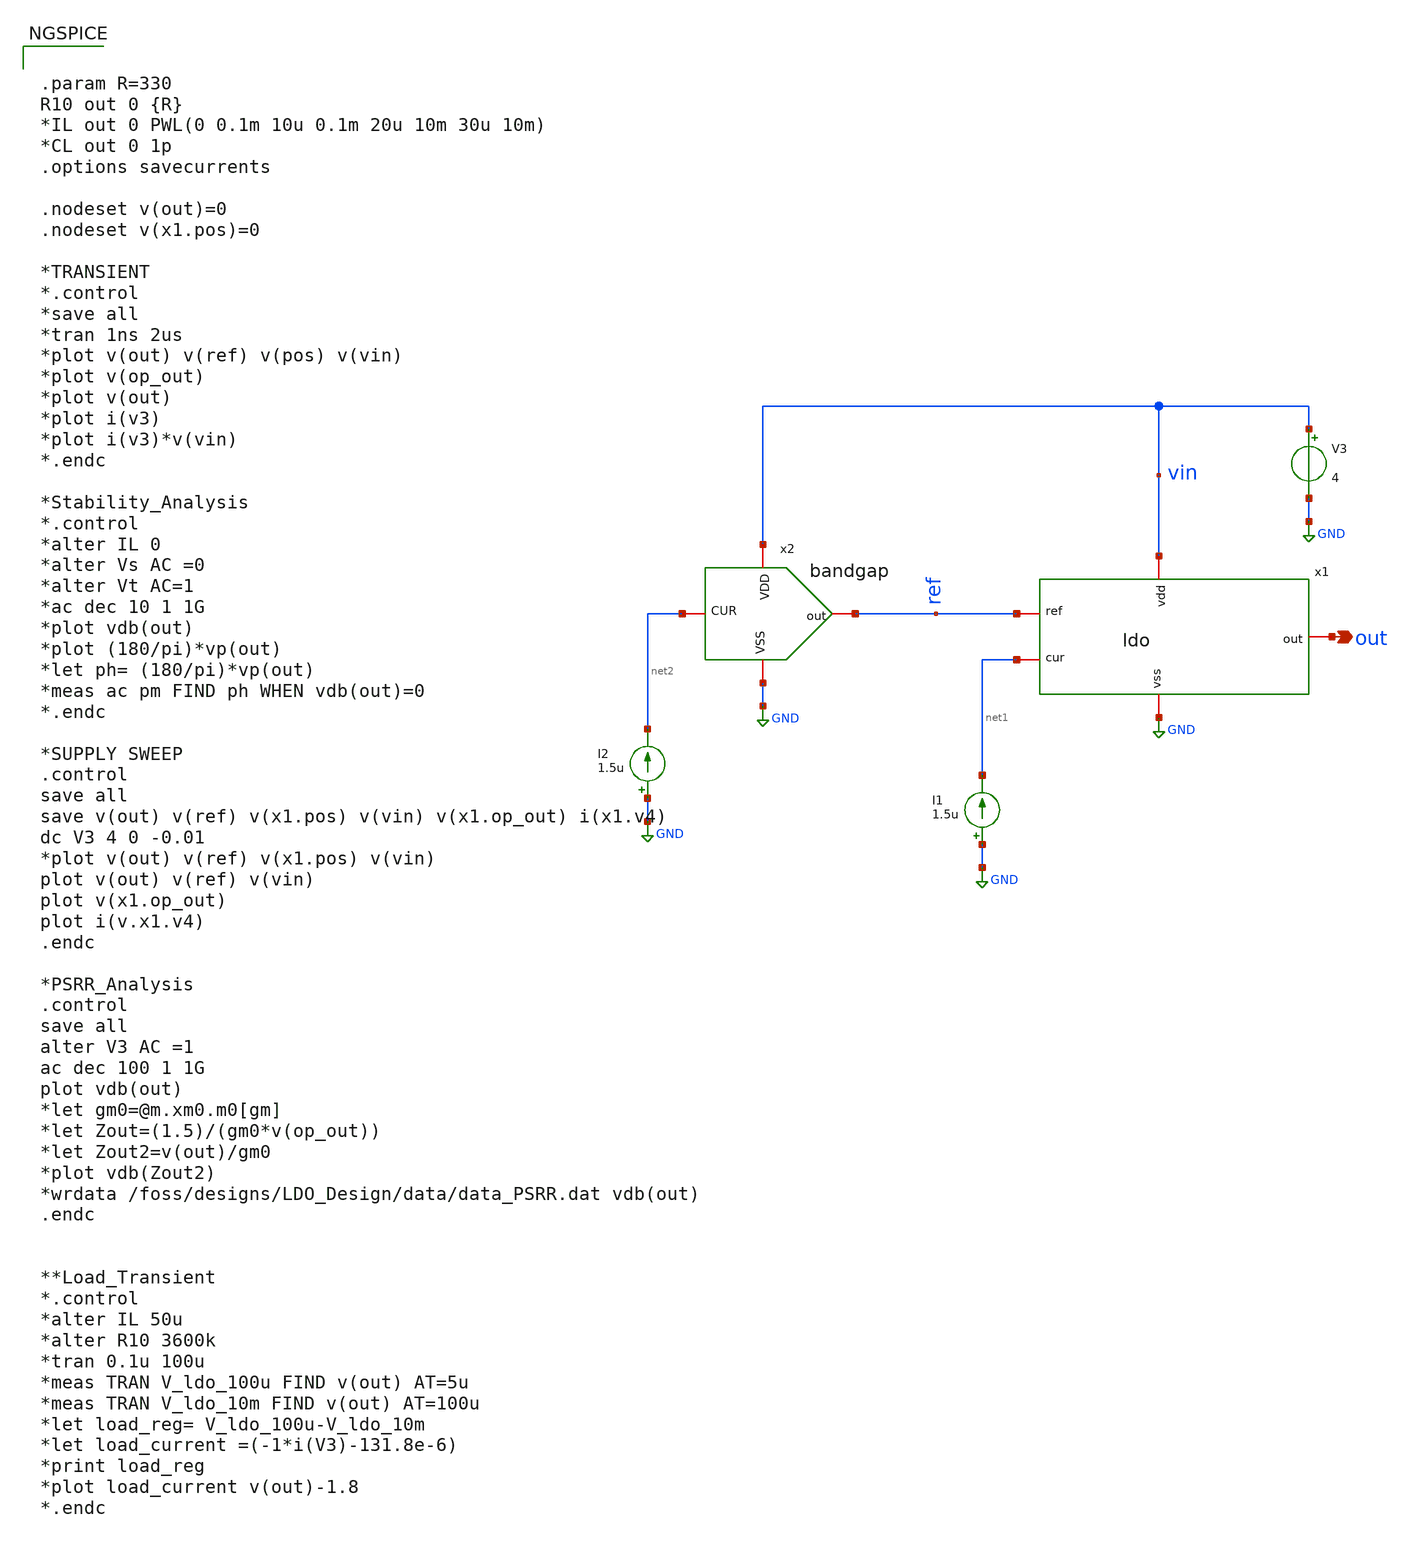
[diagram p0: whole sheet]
** sch_path: LDO/xschem/pmic/pmic-test.sch

.include $env(PDK_ROOT)/$env(PDK)/libs.tech/ngspice/design.ngspice

.lib $env(PDK_ROOT)/$env(PDK)/libs.tech/ngspice/sm141064.ngspice typical
.lib $env(PDK_ROOT)/$env(PDK)/libs.tech/ngspice/sm141064.ngspice mimcap_statistical
.lib $env(PDK_ROOT)/$env(PDK)/libs.tech/ngspice/sm141064.ngspice cap_mim
.lib $env(PDK_ROOT)/$env(PDK)/libs.tech/ngspice/sm141064.ngspice res_typical
.lib $env(PDK_ROOT)/$env(PDK)/libs.tech/ngspice/sm141064.ngspice bjt_typical
.lib $env(PDK_ROOT)/$env(PDK)/libs.tech/ngspice/sm141064.ngspice moscap_typical


**.subckt pmic-test out
*.opin out
I1 GND net1 1.5u
V3 vin GND 4
x1 vin ref net1 out GND ldo
x2 vin ref net2 GND bandgap
I2 GND net2 1.5u
**** begin user architecture code

.param R=330
R10 out 0 {R}
*IL out 0 PWL(0 0.1m 10u 0.1m 20u 10m 30u 10m)
*CL out 0 1p
.options savecurrents

.nodeset v(out)=0
.nodeset v(x1.pos)=0

*TRANSIENT
*.control
*save all
*tran 1ns 2us
*plot v(out) v(ref) v(pos) v(vin)
*plot v(op_out)
*plot v(out)
*plot i(v3)
*plot i(v3)*v(vin)
*.endc

*Stability_Analysis
*.control
*alter IL 0
*alter Vs AC =0
*alter Vt AC=1
*ac dec 10 1 1G
*plot vdb(out)
*plot (180/pi)*vp(out)
*let ph= (180/pi)*vp(out)
*meas ac pm FIND ph WHEN vdb(out)=0
*.endc

*SUPPLY SWEEP
.control
save all
save v(out) v(ref) v(x1.pos) v(vin) v(x1.op_out) i(x1.v4)
dc V3 4 0 -0.01
*plot v(out) v(ref) v(x1.pos) v(vin)
plot v(out) v(ref) v(vin)
plot v(x1.op_out)
plot i(v.x1.v4)
.endc

*PSRR_Analysis
.control
save all
alter V3 AC =1
ac dec 100 1 1G
plot vdb(out)
*let gm0=@m.xm0.m0[gm]
*let Zout=(1.5)/(gm0*v(op_out))
*let Zout2=v(out)/gm0
*plot vdb(Zout2)
*wrdata /foss/designs/LDO_Design/data/data_PSRR.dat vdb(out)
.endc


**Load_Transient
*.control
*alter IL 50u
*alter R10 3600k
*tran 0.1u 100u
*meas TRAN V_ldo_100u FIND v(out) AT=5u
*meas TRAN V_ldo_10m FIND v(out) AT=100u
*let load_reg= V_ldo_100u-V_ldo_10m
*let load_current =(-1*i(V3)-131.8e-6)
*print load_reg
*plot load_current v(out)-1.8
*.endc

**** end user architecture code
**.ends
.GLOBAL GND
.end
